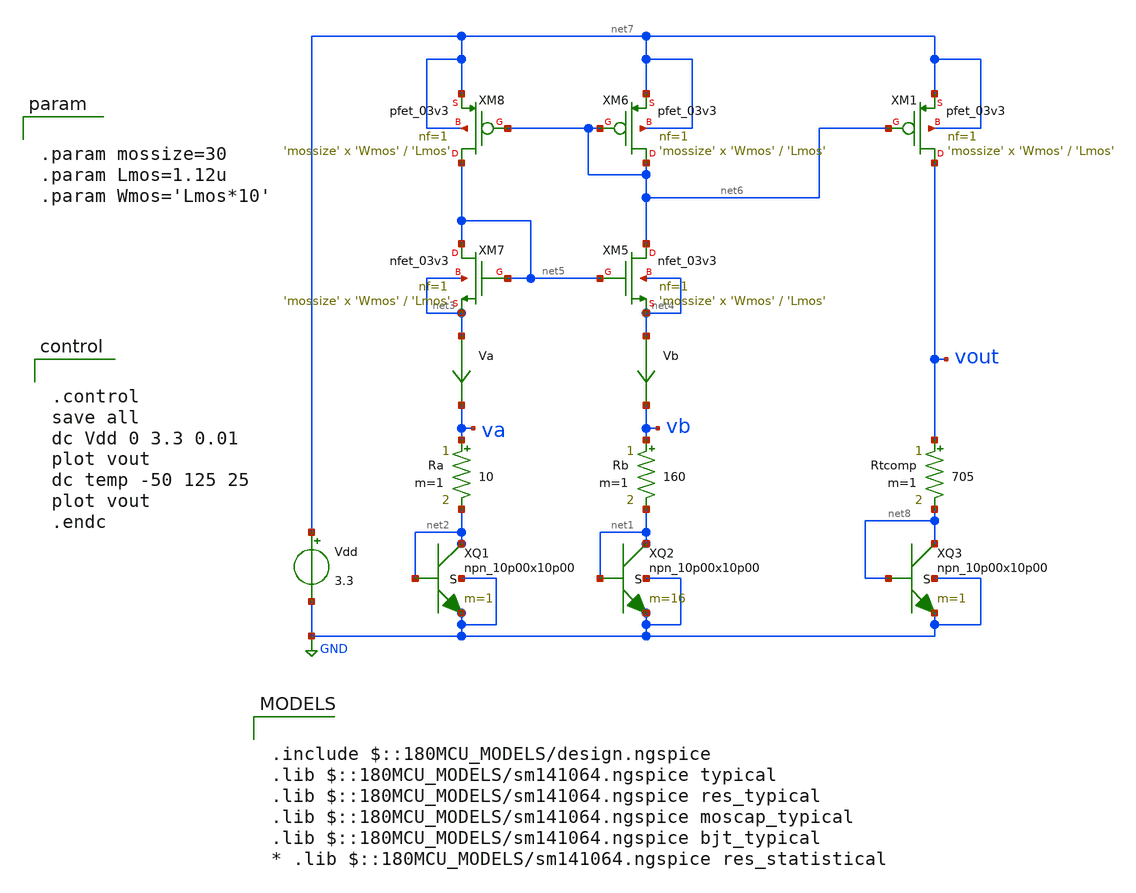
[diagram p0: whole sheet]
** sch_path: bgr-diode-currentmirror-tcomp03v3.sch
**.subckt bgr-diode-currentmirror-tcomp03v3
Vdd net7 GND 3.3
XQ1 net2 net2 GND GND npn_10p00x10p00 m=1
XQ2 net1 net1 GND GND npn_10p00x10p00 m=16
Rb vb net1 160 m=1
Ra va net2 10 m=1
Va net3 va 0
.save i(va)
Vb net4 vb 0
.save i(vb)
XM5 net6 net5 net4 net4 nfet_03v3 L='Lmos' W='Wmos' nf=1 ad='int((nf+1)/2) * W/nf * 0.18u' as='int((nf+2)/2) * W/nf * 0.18u'
+ pd='2*int((nf+1)/2) * (W/nf + 0.18u)' ps='2*int((nf+2)/2) * (W/nf + 0.18u)' nrd='0.18u / W' nrs='0.18u / W'
+ sa=0 sb=0 sd=0 m='mossize'
XM7 net5 net5 net3 net3 nfet_03v3 L='Lmos' W='Wmos' nf=1 ad='int((nf+1)/2) * W/nf * 0.18u' as='int((nf+2)/2) * W/nf * 0.18u'
+ pd='2*int((nf+1)/2) * (W/nf + 0.18u)' ps='2*int((nf+2)/2) * (W/nf + 0.18u)' nrd='0.18u / W' nrs='0.18u / W'
+ sa=0 sb=0 sd=0 m='mossize'
XM6 net6 net6 net7 net7 pfet_03v3 L='Lmos' W='Wmos' nf=1 ad='int((nf+1)/2) * W/nf * 0.18u' as='int((nf+2)/2) * W/nf * 0.18u'
+ pd='2*int((nf+1)/2) * (W/nf + 0.18u)' ps='2*int((nf+2)/2) * (W/nf + 0.18u)' nrd='0.18u / W' nrs='0.18u / W'
+ sa=0 sb=0 sd=0 m='mossize'
XM8 net5 net6 net7 net7 pfet_03v3 L='Lmos' W='Wmos' nf=1 ad='int((nf+1)/2) * W/nf * 0.18u' as='int((nf+2)/2) * W/nf * 0.18u'
+ pd='2*int((nf+1)/2) * (W/nf + 0.18u)' ps='2*int((nf+2)/2) * (W/nf + 0.18u)' nrd='0.18u / W' nrs='0.18u / W'
+ sa=0 sb=0 sd=0 m='mossize'
XM1 vout net6 net7 net7 pfet_03v3 L='Lmos' W='Wmos' nf=1 ad='int((nf+1)/2) * W/nf * 0.18u' as='int((nf+2)/2) * W/nf * 0.18u'
+ pd='2*int((nf+1)/2) * (W/nf + 0.18u)' ps='2*int((nf+2)/2) * (W/nf + 0.18u)' nrd='0.18u / W' nrs='0.18u / W'
+ sa=0 sb=0 sd=0 m='mossize'
XQ3 net8 net8 GND GND npn_10p00x10p00 m=1
Rtcomp vout net8 705 m=1
**** begin user architecture code

.include $::180MCU_MODELS/design.ngspice
.lib $::180MCU_MODELS/sm141064.ngspice typical
.lib $::180MCU_MODELS/sm141064.ngspice res_typical
.lib $::180MCU_MODELS/sm141064.ngspice moscap_typical
.lib $::180MCU_MODELS/sm141064.ngspice bjt_typical
* .lib $::180MCU_MODELS/sm141064.ngspice res_statistical



.control
save all
dc Vdd 0 3.3 0.01
plot vout
dc temp -50 125 25
plot vout
.endc




.param mossize=30
.param Lmos=1.12u
.param Wmos='Lmos*10'


**** end user architecture code
**.ends
.GLOBAL GND
.end
